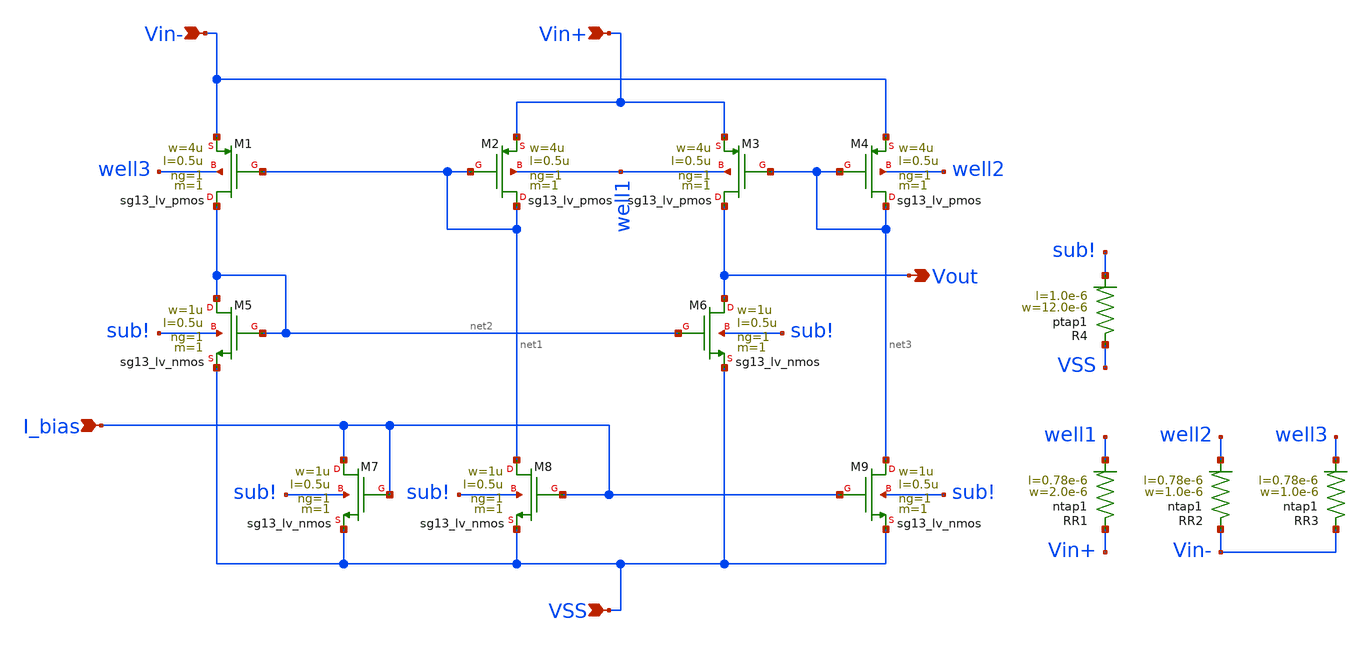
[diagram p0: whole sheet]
** sch_path: SSDOR_1.2V_v4/components/pmos_comp/pmos_comp.sch
**.subckt pmos_comp I_bias Vin- Vin+ VSS Vout
*.ipin I_bias
*.ipin Vin-
*.ipin Vin+
*.ipin VSS
*.opin Vout
XM1 net2 net1 Vin- well3 sg13_lv_pmos w=4u l=0.5u ng=1 m=1 mm_ok=1
XM2 net1 net1 Vin+ well1 sg13_lv_pmos w=4u l=0.5u ng=1 m=1 mm_ok=1
XM3 Vout net3 Vin+ well1 sg13_lv_pmos w=4u l=0.5u ng=1 m=1 mm_ok=1
XM4 net3 net3 Vin- well2 sg13_lv_pmos w=4u l=0.5u ng=1 m=1 mm_ok=1
XM5 net2 net2 VSS sub! sg13_lv_nmos w=1u l=0.5u ng=1 m=1 mm_ok=1
XM6 Vout net2 VSS sub! sg13_lv_nmos w=1u l=0.5u ng=1 m=1 mm_ok=1
XM8 net1 I_bias VSS sub! sg13_lv_nmos w=1u l=0.5u ng=1 m=1 mm_ok=1
XM7 I_bias I_bias VSS sub! sg13_lv_nmos w=1u l=0.5u ng=1 m=1 mm_ok=1
XM9 net3 I_bias VSS sub! sg13_lv_nmos w=1u l=0.5u ng=1 m=1 mm_ok=1
XR1 Vin+ well1 ntap1 R=137.6 w=2.0e-6 l=0.78e-6
XR4 VSS sub! ptap1 R=25.79 w=12.0e-6 l=1.0e-6
XR2 Vin- well2 ntap1 R=225.8 w=1.0e-6 l=0.78e-6
XR3 Vin- well3 ntap1 R=225.8 w=1.0e-6 l=0.78e-6
**.ends
.end
